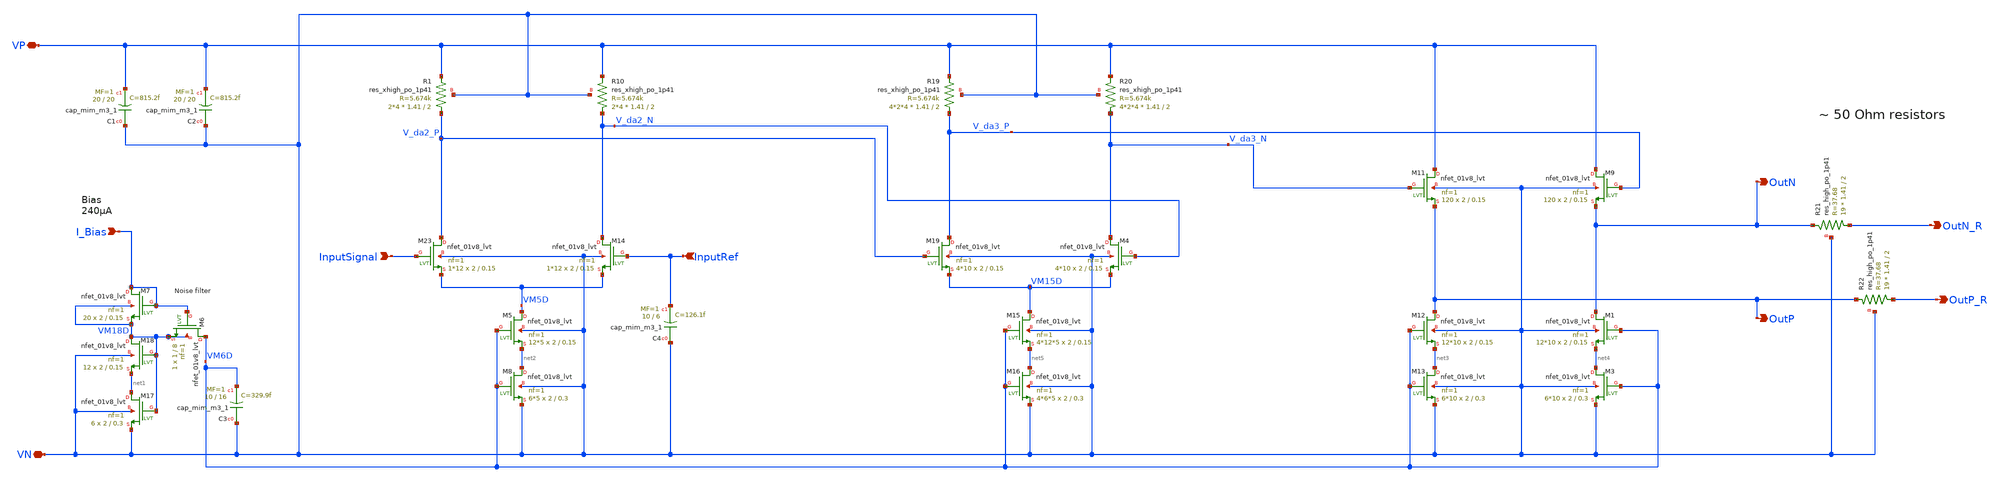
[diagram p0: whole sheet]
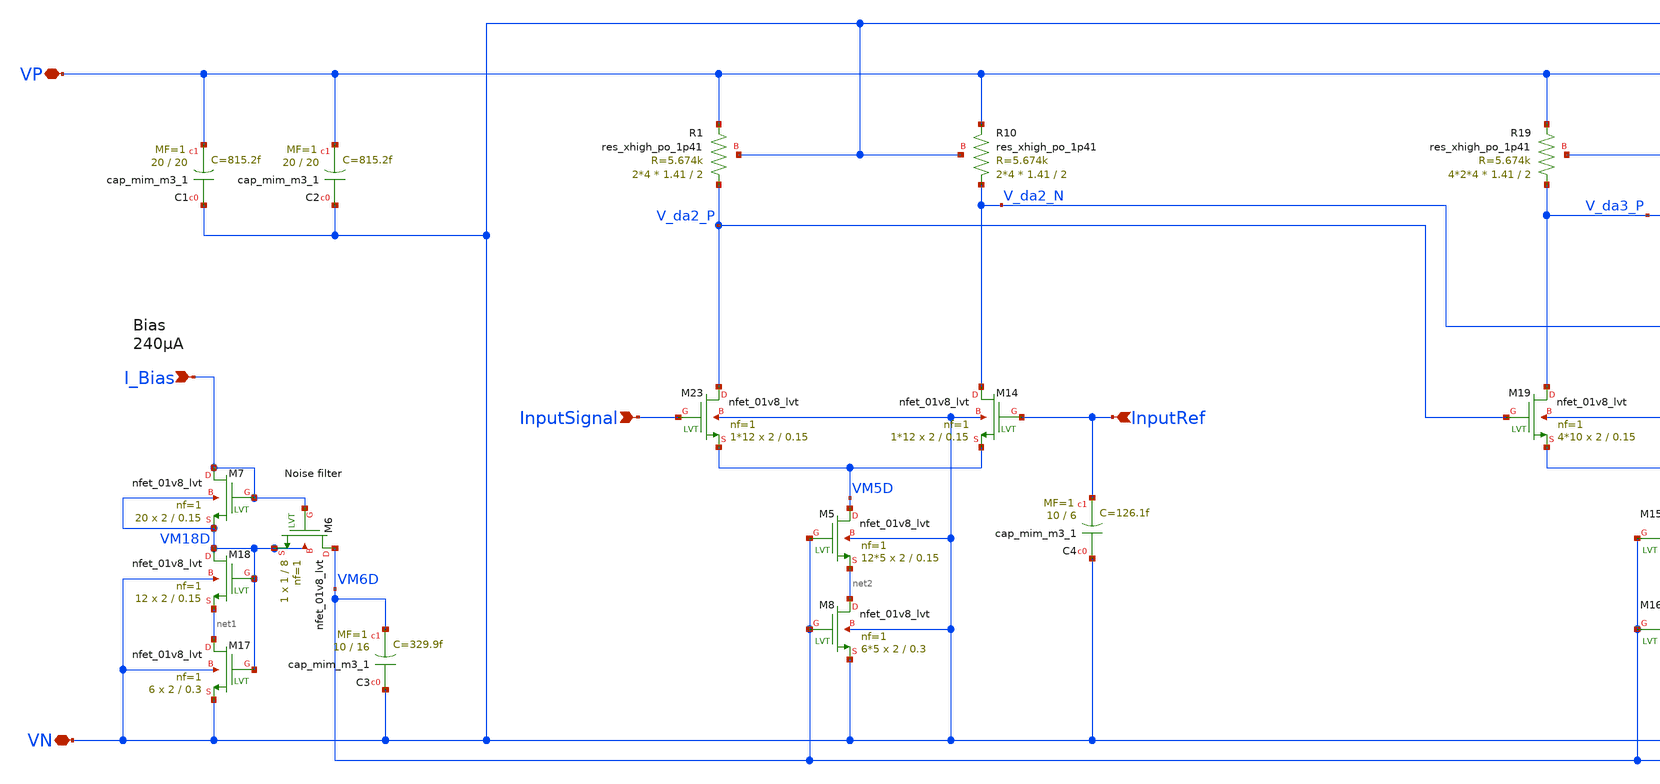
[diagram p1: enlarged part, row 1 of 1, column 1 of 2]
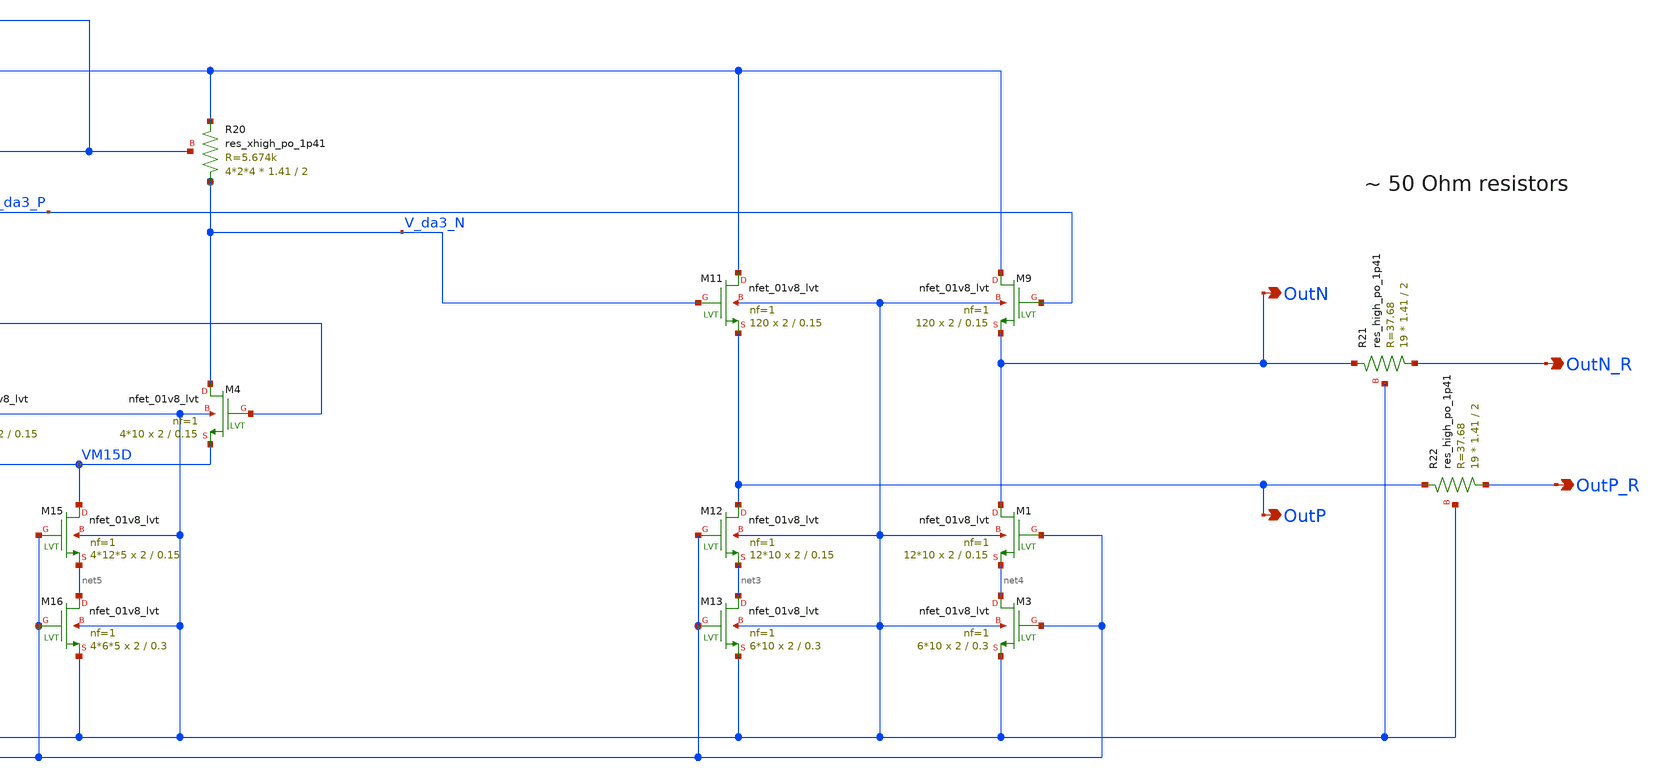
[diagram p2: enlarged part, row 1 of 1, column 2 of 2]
** sch_path: xschem/outdriver/outdriver.sch
**.subckt outdriver VN InputRef VP I_Bias InputSignal OutN OutP OutN_R OutP_R
*.iopin VN
*.ipin InputRef
*.iopin VP
*.ipin I_Bias
*.ipin InputSignal
*.opin OutN
*.opin OutP
*.opin OutN_R
*.opin OutP_R
XC3 VN VM6D sky130_fd_pr__cap_mim_m3_1 W=10 L=16 MF=1 m=1
XM17 net1 VM18D VN VN sky130_fd_pr__nfet_01v8_lvt L=0.3 W=2 nf=1 ad='int((nf+1)/2) * W/nf * 0.29' as='int((nf+2)/2) * W/nf * 0.29'
+ pd='2*int((nf+1)/2) * (W/nf + 0.29)' ps='2*int((nf+2)/2) * (W/nf + 0.29)' nrd='0.29 / W' nrs='0.29 / W'
+ sa=0 sb=0 sd=0 mult=6 m=6
XM18 VM18D VM18D net1 VN sky130_fd_pr__nfet_01v8_lvt L=0.15 W=2 nf=1 ad='int((nf+1)/2) * W/nf * 0.29'
+ as='int((nf+2)/2) * W/nf * 0.29' pd='2*int((nf+1)/2) * (W/nf + 0.29)' ps='2*int((nf+2)/2) * (W/nf + 0.29)'
+ nrd='0.29 / W' nrs='0.29 / W' sa=0 sb=0 sd=0 mult=12 m=12
XM7 I_Bias I_Bias VM18D VM18D sky130_fd_pr__nfet_01v8_lvt L=0.15 W=2 nf=1 ad='int((nf+1)/2) * W/nf * 0.29'
+ as='int((nf+2)/2) * W/nf * 0.29' pd='2*int((nf+1)/2) * (W/nf + 0.29)' ps='2*int((nf+2)/2) * (W/nf + 0.29)'
+ nrd='0.29 / W' nrs='0.29 / W' sa=0 sb=0 sd=0 mult=20 m=20
XM5 VM5D VM6D net2 VN sky130_fd_pr__nfet_01v8_lvt L=0.15 W=2 nf=1 ad='int((nf+1)/2) * W/nf * 0.29' as='int((nf+2)/2) * W/nf * 0.29'
+ pd='2*int((nf+1)/2) * (W/nf + 0.29)' ps='2*int((nf+2)/2) * (W/nf + 0.29)' nrd='0.29 / W' nrs='0.29 / W'
+ sa=0 sb=0 sd=0 mult=12*5 m=12*5
XM8 net2 VM6D VN VN sky130_fd_pr__nfet_01v8_lvt L=0.3 W=2 nf=1 ad='int((nf+1)/2) * W/nf * 0.29' as='int((nf+2)/2) * W/nf * 0.29'
+ pd='2*int((nf+1)/2) * (W/nf + 0.29)' ps='2*int((nf+2)/2) * (W/nf + 0.29)' nrd='0.29 / W' nrs='0.29 / W'
+ sa=0 sb=0 sd=0 mult=6*5 m=6*5
XM9 VP V_da3_P OutN VN sky130_fd_pr__nfet_01v8_lvt L=0.15 W=2 nf=1 ad='int((nf+1)/2) * W/nf * 0.29' as='int((nf+2)/2) * W/nf * 0.29'
+ pd='2*int((nf+1)/2) * (W/nf + 0.29)' ps='2*int((nf+2)/2) * (W/nf + 0.29)' nrd='0.29 / W' nrs='0.29 / W'
+ sa=0 sb=0 sd=0 mult=120 m=120
XM11 VP V_da3_N OutP VN sky130_fd_pr__nfet_01v8_lvt L=0.15 W=2 nf=1 ad='int((nf+1)/2) * W/nf * 0.29'
+ as='int((nf+2)/2) * W/nf * 0.29' pd='2*int((nf+1)/2) * (W/nf + 0.29)' ps='2*int((nf+2)/2) * (W/nf + 0.29)'
+ nrd='0.29 / W' nrs='0.29 / W' sa=0 sb=0 sd=0 mult=120 m=120
XM12 OutP VM6D net3 VN sky130_fd_pr__nfet_01v8_lvt L=0.15 W=2 nf=1 ad='int((nf+1)/2) * W/nf * 0.29' as='int((nf+2)/2) * W/nf * 0.29'
+ pd='2*int((nf+1)/2) * (W/nf + 0.29)' ps='2*int((nf+2)/2) * (W/nf + 0.29)' nrd='0.29 / W' nrs='0.29 / W'
+ sa=0 sb=0 sd=0 mult=12*10 m=12*10
XM13 net3 VM6D VN VN sky130_fd_pr__nfet_01v8_lvt L=0.3 W=2 nf=1 ad='int((nf+1)/2) * W/nf * 0.29' as='int((nf+2)/2) * W/nf * 0.29'
+ pd='2*int((nf+1)/2) * (W/nf + 0.29)' ps='2*int((nf+2)/2) * (W/nf + 0.29)' nrd='0.29 / W' nrs='0.29 / W'
+ sa=0 sb=0 sd=0 mult=6*10 m=6*10
XM1 OutN VM6D net4 VN sky130_fd_pr__nfet_01v8_lvt L=0.15 W=2 nf=1 ad='int((nf+1)/2) * W/nf * 0.29' as='int((nf+2)/2) * W/nf * 0.29'
+ pd='2*int((nf+1)/2) * (W/nf + 0.29)' ps='2*int((nf+2)/2) * (W/nf + 0.29)' nrd='0.29 / W' nrs='0.29 / W'
+ sa=0 sb=0 sd=0 mult=12*10 m=12*10
XM3 net4 VM6D VN VN sky130_fd_pr__nfet_01v8_lvt L=0.3 W=2 nf=1 ad='int((nf+1)/2) * W/nf * 0.29' as='int((nf+2)/2) * W/nf * 0.29'
+ pd='2*int((nf+1)/2) * (W/nf + 0.29)' ps='2*int((nf+2)/2) * (W/nf + 0.29)' nrd='0.29 / W' nrs='0.29 / W'
+ sa=0 sb=0 sd=0 mult=6*10 m=6*10
XM6 VM6D I_Bias VM18D VM18D sky130_fd_pr__nfet_01v8_lvt L=8 W=1 nf=1 ad='int((nf+1)/2) * W/nf * 0.29'
+ as='int((nf+2)/2) * W/nf * 0.29' pd='2*int((nf+1)/2) * (W/nf + 0.29)' ps='2*int((nf+2)/2) * (W/nf + 0.29)'
+ nrd='0.29 / W' nrs='0.29 / W' sa=0 sb=0 sd=0 mult=1 m=1
XC1 VN VP sky130_fd_pr__cap_mim_m3_1 W=20 L=20 MF=1 m=1
XC2 VN VP sky130_fd_pr__cap_mim_m3_1 W=20 L=20 MF=1 m=1
XM15 VM15D VM6D net5 VN sky130_fd_pr__nfet_01v8_lvt L=0.15 W=2 nf=1 ad='int((nf+1)/2) * W/nf * 0.29'
+ as='int((nf+2)/2) * W/nf * 0.29' pd='2*int((nf+1)/2) * (W/nf + 0.29)' ps='2*int((nf+2)/2) * (W/nf + 0.29)'
+ nrd='0.29 / W' nrs='0.29 / W' sa=0 sb=0 sd=0 mult=4*12*5 m=4*12*5
XM16 net5 VM6D VN VN sky130_fd_pr__nfet_01v8_lvt L=0.3 W=2 nf=1 ad='int((nf+1)/2) * W/nf * 0.29' as='int((nf+2)/2) * W/nf * 0.29'
+ pd='2*int((nf+1)/2) * (W/nf + 0.29)' ps='2*int((nf+2)/2) * (W/nf + 0.29)' nrd='0.29 / W' nrs='0.29 / W'
+ sa=0 sb=0 sd=0 mult=4*6*5 m=4*6*5
XR19 V_da3_P VP VN sky130_fd_pr__res_xhigh_po_1p41 L=2 mult=4*2*4 m=4*2*4
XR20 V_da3_N VP VN sky130_fd_pr__res_xhigh_po_1p41 L=2 mult=4*2*4 m=4*2*4
XM4 V_da3_N V_da2_N VM15D VN sky130_fd_pr__nfet_01v8_lvt L=0.15 W=2 nf=1 ad='int((nf+1)/2) * W/nf * 0.29'
+ as='int((nf+2)/2) * W/nf * 0.29' pd='2*int((nf+1)/2) * (W/nf + 0.29)' ps='2*int((nf+2)/2) * (W/nf + 0.29)'
+ nrd='0.29 / W' nrs='0.29 / W' sa=0 sb=0 sd=0 mult=4*10 m=4*10
XR21 OutN_R OutN VN sky130_fd_pr__res_high_po_1p41 L=2 mult=19 m=19
XR22 OutP_R OutP VN sky130_fd_pr__res_high_po_1p41 L=2 mult=19 m=19
XM23 V_da2_P InputSignal VM5D VN sky130_fd_pr__nfet_01v8_lvt L=0.15 W=2 nf=1 ad='int((nf+1)/2) * W/nf * 0.29'
+ as='int((nf+2)/2) * W/nf * 0.29' pd='2*int((nf+1)/2) * (W/nf + 0.29)' ps='2*int((nf+2)/2) * (W/nf + 0.29)'
+ nrd='0.29 / W' nrs='0.29 / W' sa=0 sb=0 sd=0 mult=1*12 m=1*12
XM19 V_da3_P V_da2_P VM15D VN sky130_fd_pr__nfet_01v8_lvt L=0.15 W=2 nf=1 ad='int((nf+1)/2) * W/nf * 0.29'
+ as='int((nf+2)/2) * W/nf * 0.29' pd='2*int((nf+1)/2) * (W/nf + 0.29)' ps='2*int((nf+2)/2) * (W/nf + 0.29)'
+ nrd='0.29 / W' nrs='0.29 / W' sa=0 sb=0 sd=0 mult=4*10 m=4*10
XM14 V_da2_N InputRef VM5D VN sky130_fd_pr__nfet_01v8_lvt L=0.15 W=2 nf=1 ad='int((nf+1)/2) * W/nf * 0.29'
+ as='int((nf+2)/2) * W/nf * 0.29' pd='2*int((nf+1)/2) * (W/nf + 0.29)' ps='2*int((nf+2)/2) * (W/nf + 0.29)'
+ nrd='0.29 / W' nrs='0.29 / W' sa=0 sb=0 sd=0 mult=1*12 m=1*12
XR1 V_da2_P VP VN sky130_fd_pr__res_xhigh_po_1p41 L=2 mult=2*4 m=2*4
XR10 V_da2_N VP VN sky130_fd_pr__res_xhigh_po_1p41 L=2 mult=2*4 m=2*4
XC4 VN InputRef sky130_fd_pr__cap_mim_m3_1 W=10 L=6 MF=1 m=1
**.ends
.end
